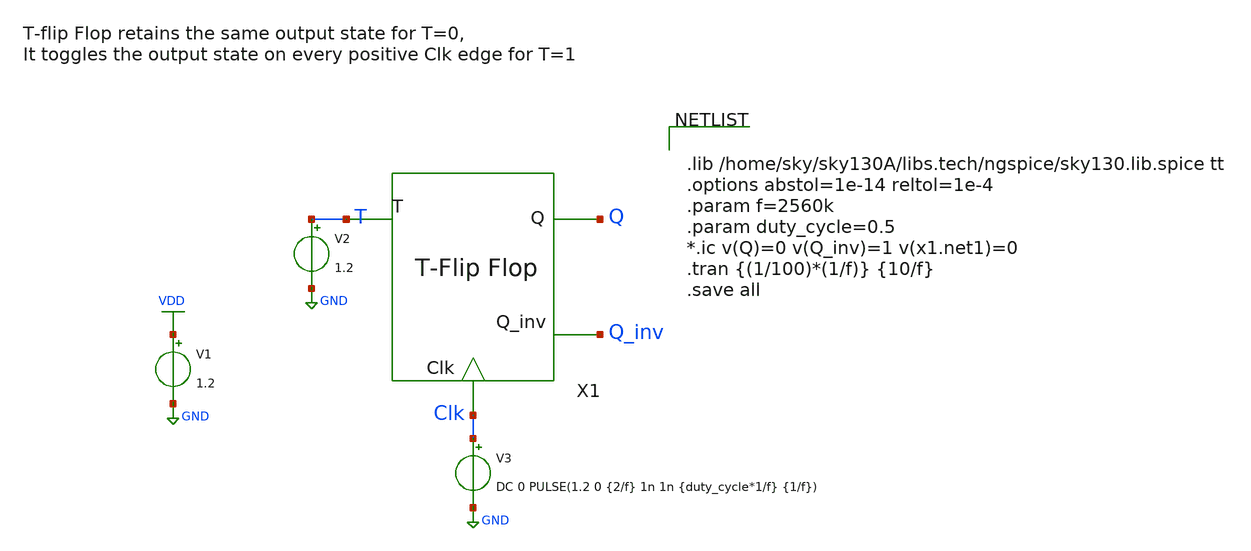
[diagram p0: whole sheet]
** sch_path: xschem/T_flip_flop/T_flip_flop_tb.sch
**.subckt T_flip_flop_tb
X1 T Q Q_inv Clk T_flip_flop
V1 VDD GND 1.2
V3 Clk GND DC 0 PULSE(1.2 0 {2/f} 1n 1n {duty_cycle*1/f} {1/f})
V2 T GND 1.2
**** begin user architecture code


.lib /home/sky/sky130A/libs.tech/ngspice/sky130.lib.spice tt
.options abstol=1e-14 reltol=1e-4
.param f=2560k
.param duty_cycle=0.5
*.ic v(Q)=0 v(Q_inv)=1 v(x1.net1)=0
.tran {(1/100)*(1/f)} {10/f}
.save all


**** end user architecture code
**.ends

* expanding   symbol:  T_flip_flop/T_flip_flop.sym # of pins=4
** sym_path: xschem/T_flip_flop/T_flip_flop.sym
** sch_path: xschem/T_flip_flop/T_flip_flop.sch
.subckt T_flip_flop T Q Q_inv Clk
*.ipin T
*.ipin Clk
*.opin Q
*.opin Q_inv
X1 net1 Q Q_inv Clk d_flip_flop
X2 Q T net1 exor_gate
.ends


* expanding   symbol:  D_flip_flop/d_flip_flop.sym # of pins=4
** sym_path: xschem/D_flip_flop/d_flip_flop.sym
** sch_path: xschem/D_flip_flop/d_flip_flop.sch
.subckt d_flip_flop D Q Q_inv Clk
*.ipin D
*.ipin Clk
*.opin Q_inv
*.opin Q
X1 net1 net2 inv Wpmos=3 Lpmos=0.18 Wnmos=1 Lnmos=0.18
X2 net3 Q inv Wpmos=3 Lpmos=0.18 Wnmos=1 Lnmos=0.18
X3 net2 net4 inv Wpmos=3 Lpmos=0.18 Wnmos=1 Lnmos=0.18
X4 Q Q_inv inv Wpmos=3 Lpmos=0.18 Wnmos=1 Lnmos=0.18
X5 D net1 Clk Clk_inv transmission_gate Wpmos=1 Lpmos=0.18 Wnmos=1 Lnmos=0.18
X6 net1 net4 Clk_inv Clk transmission_gate Wpmos=1 Lpmos=0.18 Wnmos=1 Lnmos=0.18
X7 net3 Q_inv Clk Clk_inv transmission_gate Wpmos=1 Lpmos=0.18 Wnmos=1 Lnmos=0.18
X8 net2 net3 Clk_inv Clk transmission_gate Wpmos=1 Lpmos=0.18 Wnmos=1 Lnmos=0.18
X9 Clk Clk_inv inv Wpmos=3 Lpmos=0.18 Wnmos=1 Lnmos=0.18
.ends


* expanding   symbol:  exor_gate/exor_gate.sym # of pins=3
** sym_path: xschem/exor_gate/exor_gate.sym
** sch_path: xschem/exor_gate/exor_gate.sch
.subckt exor_gate A B out
*.ipin A
*.ipin B
*.opin out
XM4 out A net1 GND sky130_fd_pr__nfet_01v8 L=0.18 W=0.5 nf=1 ad='int((nf+1)/2) * W/nf * 0.29' as='int((nf+2)/2) * W/nf * 0.29'
+ pd='2*int((nf+1)/2) * (W/nf + 0.29)' ps='2*int((nf+2)/2) * (W/nf + 0.29)' nrd='0.29 / W' nrs='0.29 / W'
+ sa=0 sb=0 sd=0 mult=1 m=1
XM5 net3 B VDD VDD sky130_fd_pr__pfet_01v8 L=0.18 W=1 nf=1 ad='int((nf+1)/2) * W/nf * 0.29' as='int((nf+2)/2) * W/nf * 0.29'
+ pd='2*int((nf+1)/2) * (W/nf + 0.29)' ps='2*int((nf+2)/2) * (W/nf + 0.29)' nrd='0.29 / W' nrs='0.29 / W'
+ sa=0 sb=0 sd=0 mult=1 m=1
XM1 net1 B GND GND sky130_fd_pr__nfet_01v8 L=0.18 W=0.5 nf=1 ad='int((nf+1)/2) * W/nf * 0.29' as='int((nf+2)/2) * W/nf * 0.29'
+ pd='2*int((nf+1)/2) * (W/nf + 0.29)' ps='2*int((nf+2)/2) * (W/nf + 0.29)' nrd='0.29 / W' nrs='0.29 / W'
+ sa=0 sb=0 sd=0 mult=1 m=1
XM2 out net5 net3 VDD sky130_fd_pr__pfet_01v8 L=0.18 W=1 nf=1 ad='int((nf+1)/2) * W/nf * 0.29' as='int((nf+2)/2) * W/nf * 0.29'
+ pd='2*int((nf+1)/2) * (W/nf + 0.29)' ps='2*int((nf+2)/2) * (W/nf + 0.29)' nrd='0.29 / W' nrs='0.29 / W'
+ sa=0 sb=0 sd=0 mult=1 m=1
XM3 net4 net6 VDD VDD sky130_fd_pr__pfet_01v8 L=0.18 W=1 nf=1 ad='int((nf+1)/2) * W/nf * 0.29' as='int((nf+2)/2) * W/nf * 0.29'
+ pd='2*int((nf+1)/2) * (W/nf + 0.29)' ps='2*int((nf+2)/2) * (W/nf + 0.29)' nrd='0.29 / W' nrs='0.29 / W'
+ sa=0 sb=0 sd=0 mult=1 m=1
XM6 out A net4 VDD sky130_fd_pr__pfet_01v8 L=0.18 W=1 nf=1 ad='int((nf+1)/2) * W/nf * 0.29' as='int((nf+2)/2) * W/nf * 0.29'
+ pd='2*int((nf+1)/2) * (W/nf + 0.29)' ps='2*int((nf+2)/2) * (W/nf + 0.29)' nrd='0.29 / W' nrs='0.29 / W'
+ sa=0 sb=0 sd=0 mult=1 m=1
XM7 out net5 net2 GND sky130_fd_pr__nfet_01v8 L=0.18 W=0.5 nf=1 ad='int((nf+1)/2) * W/nf * 0.29' as='int((nf+2)/2) * W/nf * 0.29'
+ pd='2*int((nf+1)/2) * (W/nf + 0.29)' ps='2*int((nf+2)/2) * (W/nf + 0.29)' nrd='0.29 / W' nrs='0.29 / W'
+ sa=0 sb=0 sd=0 mult=1 m=1
XM8 net2 net6 GND GND sky130_fd_pr__nfet_01v8 L=0.18 W=0.5 nf=1 ad='int((nf+1)/2) * W/nf * 0.29' as='int((nf+2)/2) * W/nf * 0.29'
+ pd='2*int((nf+1)/2) * (W/nf + 0.29)' ps='2*int((nf+2)/2) * (W/nf + 0.29)' nrd='0.29 / W' nrs='0.29 / W'
+ sa=0 sb=0 sd=0 mult=1 m=1
X3 B net6 inv Wpmos=3 Lpmos=0.18 Wnmos=1 Lnmos=0.18
X2 A net5 inv Wpmos=3 Lpmos=0.18 Wnmos=1 Lnmos=0.18
.ends


* expanding   symbol:  inv/inv.sym # of pins=2
** sym_path: xschem/inv/inv.sym
** sch_path: xschem/inv/inv.sch
.subckt inv in out  Wpmos=3 Lpmos=0.18 Wnmos=1 Lnmos=0.18
*.ipin in
*.iopin out
XM1 out in GND GND sky130_fd_pr__nfet_01v8 L=Lnmos W=Wnmos nf=1 ad='int((nf+1)/2) * W/nf * 0.29' as='int((nf+2)/2) * W/nf * 0.29'
+ pd='2*int((nf+1)/2) * (W/nf + 0.29)' ps='2*int((nf+2)/2) * (W/nf + 0.29)' nrd='0.29 / W' nrs='0.29 / W'
+ sa=0 sb=0 sd=0 mult=1 m=1
XM2 out in VDD VDD sky130_fd_pr__pfet_01v8 L=Lpmos W=Wpmos nf=1 ad='int((nf+1)/2) * W/nf * 0.29' as='int((nf+2)/2) * W/nf * 0.29'
+ pd='2*int((nf+1)/2) * (W/nf + 0.29)' ps='2*int((nf+2)/2) * (W/nf + 0.29)' nrd='0.29 / W' nrs='0.29 / W'
+ sa=0 sb=0 sd=0 mult=1 m=1
.ends


* expanding   symbol:  transmission_gate/transmission_gate.sym # of pins=4
** sym_path: xschem/transmission_gate/transmission_gate.sym
** sch_path: xschem/transmission_gate/transmission_gate.sch
.subckt transmission_gate in out ctrl_ ctrl  Wpmos=1 Lpmos=0.18 Wnmos=1 Lnmos=0.18
*.iopin in
*.iopin out
*.ipin ctrl_
*.ipin ctrl
XM1 in ctrl out GND sky130_fd_pr__nfet_01v8 L=Lnmos W=Wnmos nf=1 ad='int((nf+1)/2) * W/nf * 0.29' as='int((nf+2)/2) * W/nf * 0.29'
+ pd='2*int((nf+1)/2) * (W/nf + 0.29)' ps='2*int((nf+2)/2) * (W/nf + 0.29)' nrd='0.29 / W' nrs='0.29 / W'
+ sa=0 sb=0 sd=0 mult=1 m=1
XM2 out ctrl_ in VDD sky130_fd_pr__pfet_01v8 L=Lpmos W=Wpmos nf=1 ad='int((nf+1)/2) * W/nf * 0.29' as='int((nf+2)/2) * W/nf * 0.29'
+ pd='2*int((nf+1)/2) * (W/nf + 0.29)' ps='2*int((nf+2)/2) * (W/nf + 0.29)' nrd='0.29 / W' nrs='0.29 / W'
+ sa=0 sb=0 sd=0 mult=1 m=1
.ends

.GLOBAL VDD
.GLOBAL GND
.end
